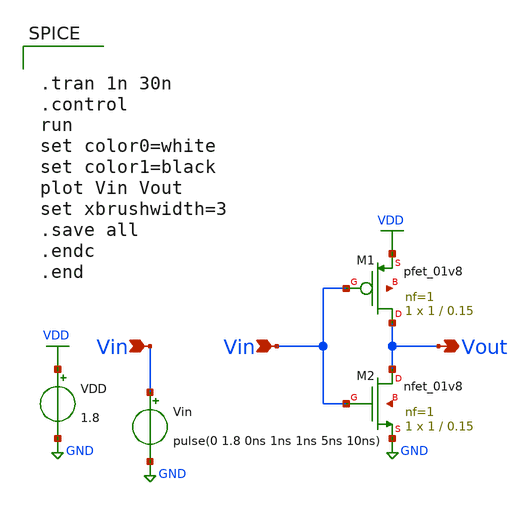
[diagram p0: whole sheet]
** sch_path: xschem/Transient_Analysis_Inverter.sch
**.subckt Transient_Analysis_Inverter Vin Vin Vout
*.ipin Vin
*.ipin Vin
*.opin Vout
VDD VDD GND 1.8
Vin Vin GND pulse(0 1.8 0ns 1ns 1ns 5ns 10ns)
XM1 Vout Vin VDD net1 sky130_fd_pr__pfet_01v8 L=0.15 W=1 nf=1 ad='int((nf+1)/2) * W/nf * 0.29' as='int((nf+2)/2) * W/nf * 0.29'
+ pd='2*int((nf+1)/2) * (W/nf + 0.29)' ps='2*int((nf+2)/2) * (W/nf + 0.29)' nrd='0.29 / W' nrs='0.29 / W'
+ sa=0 sb=0 sd=0 mult=1 m=1
XM2 Vout Vin GND net2 sky130_fd_pr__nfet_01v8 L=0.15 W=1 nf=1 ad='int((nf+1)/2) * W/nf * 0.29' as='int((nf+2)/2) * W/nf * 0.29'
+ pd='2*int((nf+1)/2) * (W/nf + 0.29)' ps='2*int((nf+2)/2) * (W/nf + 0.29)' nrd='0.29 / W' nrs='0.29 / W'
+ sa=0 sb=0 sd=0 mult=1 m=1
**** begin user architecture code


.lib /usr/local/share/pdk/sky130A/libs.tech/ngspice/sky130.lib.spice tt

.save all





.tran 1n 30n
.control
run
set color0=white
set color1=black
plot Vin Vout
set xbrushwidth=3
.save all
.endc
.end


**** end user architecture code
**.ends
.GLOBAL VDD
.GLOBAL GND
.end
